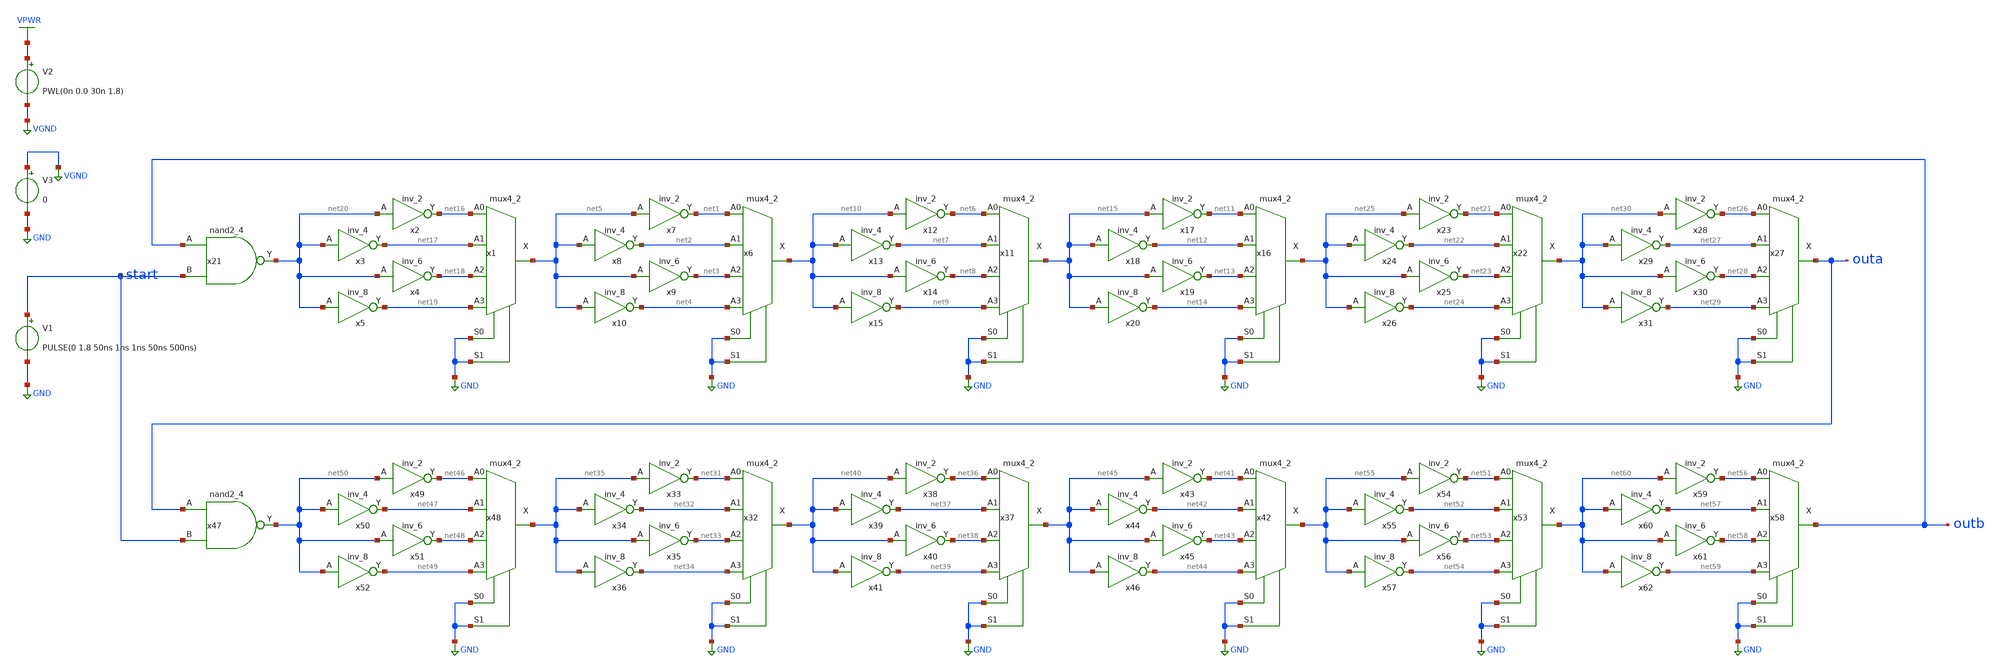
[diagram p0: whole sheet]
** sch_path: ip/randsack/sch/unstablering.sch
**.subckt unstablering
V1 start GND PULSE(0 1.8 50ns 1ns 1ns 50ns 500ns)
x6 net1 net2 net3 net4 GND GND VGND VNB VPB VPWR net10 sky130_fd_sc_hd__mux4_2
x7 net5 VGND VNB VPB VPWR net1 sky130_fd_sc_hd__inv_2
x8 net5 VGND VNB VPB VPWR net2 sky130_fd_sc_hd__inv_4
x9 net5 VGND VNB VPB VPWR net3 sky130_fd_sc_hd__inv_6
x10 net5 VGND VNB VPB VPWR net4 sky130_fd_sc_hd__inv_8
x11 net6 net7 net8 net9 GND GND VGND VNB VPB VPWR net15 sky130_fd_sc_hd__mux4_2
x12 net10 VGND VNB VPB VPWR net6 sky130_fd_sc_hd__inv_2
x13 net10 VGND VNB VPB VPWR net7 sky130_fd_sc_hd__inv_4
x14 net10 VGND VNB VPB VPWR net8 sky130_fd_sc_hd__inv_6
x15 net10 VGND VNB VPB VPWR net9 sky130_fd_sc_hd__inv_8
x16 net11 net12 net13 net14 GND GND VGND VNB VPB VPWR net25 sky130_fd_sc_hd__mux4_2
x17 net15 VGND VNB VPB VPWR net11 sky130_fd_sc_hd__inv_2
x18 net15 VGND VNB VPB VPWR net12 sky130_fd_sc_hd__inv_4
x19 net15 VGND VNB VPB VPWR net13 sky130_fd_sc_hd__inv_6
x20 net15 VGND VNB VPB VPWR net14 sky130_fd_sc_hd__inv_8
x21 outb start VGND VNB VPB VPWR net20 sky130_fd_sc_hd__nand2_4
x1 net16 net17 net18 net19 GND GND VGND VNB VPB VPWR net5 sky130_fd_sc_hd__mux4_2
x2 net20 VGND VNB VPB VPWR net16 sky130_fd_sc_hd__inv_2
x3 net20 VGND VNB VPB VPWR net17 sky130_fd_sc_hd__inv_4
x4 net20 VGND VNB VPB VPWR net18 sky130_fd_sc_hd__inv_6
x5 net20 VGND VNB VPB VPWR net19 sky130_fd_sc_hd__inv_8
x22 net21 net22 net23 net24 GND GND VGND VNB VPB VPWR net30 sky130_fd_sc_hd__mux4_2
x23 net25 VGND VNB VPB VPWR net21 sky130_fd_sc_hd__inv_2
x24 net25 VGND VNB VPB VPWR net22 sky130_fd_sc_hd__inv_4
x25 net25 VGND VNB VPB VPWR net23 sky130_fd_sc_hd__inv_6
x26 net25 VGND VNB VPB VPWR net24 sky130_fd_sc_hd__inv_8
x27 net26 net27 net28 net29 GND GND VGND VNB VPB VPWR outa sky130_fd_sc_hd__mux4_2
x28 net30 VGND VNB VPB VPWR net26 sky130_fd_sc_hd__inv_2
x29 net30 VGND VNB VPB VPWR net27 sky130_fd_sc_hd__inv_4
x30 net30 VGND VNB VPB VPWR net28 sky130_fd_sc_hd__inv_6
x31 net30 VGND VNB VPB VPWR net29 sky130_fd_sc_hd__inv_8
V2 VPWR VGND PWL(0n 0.0 30n 1.8)
x32 net31 net32 net33 net34 GND GND VGND VNB VPB VPWR net40 sky130_fd_sc_hd__mux4_2
x33 net35 VGND VNB VPB VPWR net31 sky130_fd_sc_hd__inv_2
x34 net35 VGND VNB VPB VPWR net32 sky130_fd_sc_hd__inv_4
x35 net35 VGND VNB VPB VPWR net33 sky130_fd_sc_hd__inv_6
x36 net35 VGND VNB VPB VPWR net34 sky130_fd_sc_hd__inv_8
x37 net36 net37 net38 net39 GND GND VGND VNB VPB VPWR net45 sky130_fd_sc_hd__mux4_2
x38 net40 VGND VNB VPB VPWR net36 sky130_fd_sc_hd__inv_2
x39 net40 VGND VNB VPB VPWR net37 sky130_fd_sc_hd__inv_4
x40 net40 VGND VNB VPB VPWR net38 sky130_fd_sc_hd__inv_6
x41 net40 VGND VNB VPB VPWR net39 sky130_fd_sc_hd__inv_8
x42 net41 net42 net43 net44 GND GND VGND VNB VPB VPWR net55 sky130_fd_sc_hd__mux4_2
x43 net45 VGND VNB VPB VPWR net41 sky130_fd_sc_hd__inv_2
x44 net45 VGND VNB VPB VPWR net42 sky130_fd_sc_hd__inv_4
x45 net45 VGND VNB VPB VPWR net43 sky130_fd_sc_hd__inv_6
x46 net45 VGND VNB VPB VPWR net44 sky130_fd_sc_hd__inv_8
x47 outa start VGND VNB VPB VPWR net50 sky130_fd_sc_hd__nand2_4
x48 net46 net47 net48 net49 GND GND VGND VNB VPB VPWR net35 sky130_fd_sc_hd__mux4_2
x49 net50 VGND VNB VPB VPWR net46 sky130_fd_sc_hd__inv_2
x50 net50 VGND VNB VPB VPWR net47 sky130_fd_sc_hd__inv_4
x51 net50 VGND VNB VPB VPWR net48 sky130_fd_sc_hd__inv_6
x52 net50 VGND VNB VPB VPWR net49 sky130_fd_sc_hd__inv_8
x53 net51 net52 net53 net54 GND GND VGND VNB VPB VPWR net60 sky130_fd_sc_hd__mux4_2
x54 net55 VGND VNB VPB VPWR net51 sky130_fd_sc_hd__inv_2
x55 net55 VGND VNB VPB VPWR net52 sky130_fd_sc_hd__inv_4
x56 net55 VGND VNB VPB VPWR net53 sky130_fd_sc_hd__inv_6
x57 net55 VGND VNB VPB VPWR net54 sky130_fd_sc_hd__inv_8
x58 net56 net57 net58 net59 GND GND VGND VNB VPB VPWR outb sky130_fd_sc_hd__mux4_2
x59 net60 VGND VNB VPB VPWR net56 sky130_fd_sc_hd__inv_2
x60 net60 VGND VNB VPB VPWR net57 sky130_fd_sc_hd__inv_4
x61 net60 VGND VNB VPB VPWR net58 sky130_fd_sc_hd__inv_6
x62 net60 VGND VNB VPB VPWR net59 sky130_fd_sc_hd__inv_8
V3 VGND GND 0
**** begin user architecture code


.lib /home/harrison/workspace/sky130/sky130A/libs.tech/ngspice/sky130.lib.spice tt
.include /home/harrison/workspace/sky130/sky130A/libs.ref/sky130_fd_sc_hd/spice/sky130_fd_sc_hd.spice

.control
save all
tran 0.1n 1u
write unstablering.out
.endc


**** end user architecture code
**.ends
.GLOBAL GND
.GLOBAL VPWR
.GLOBAL VGND
.end
